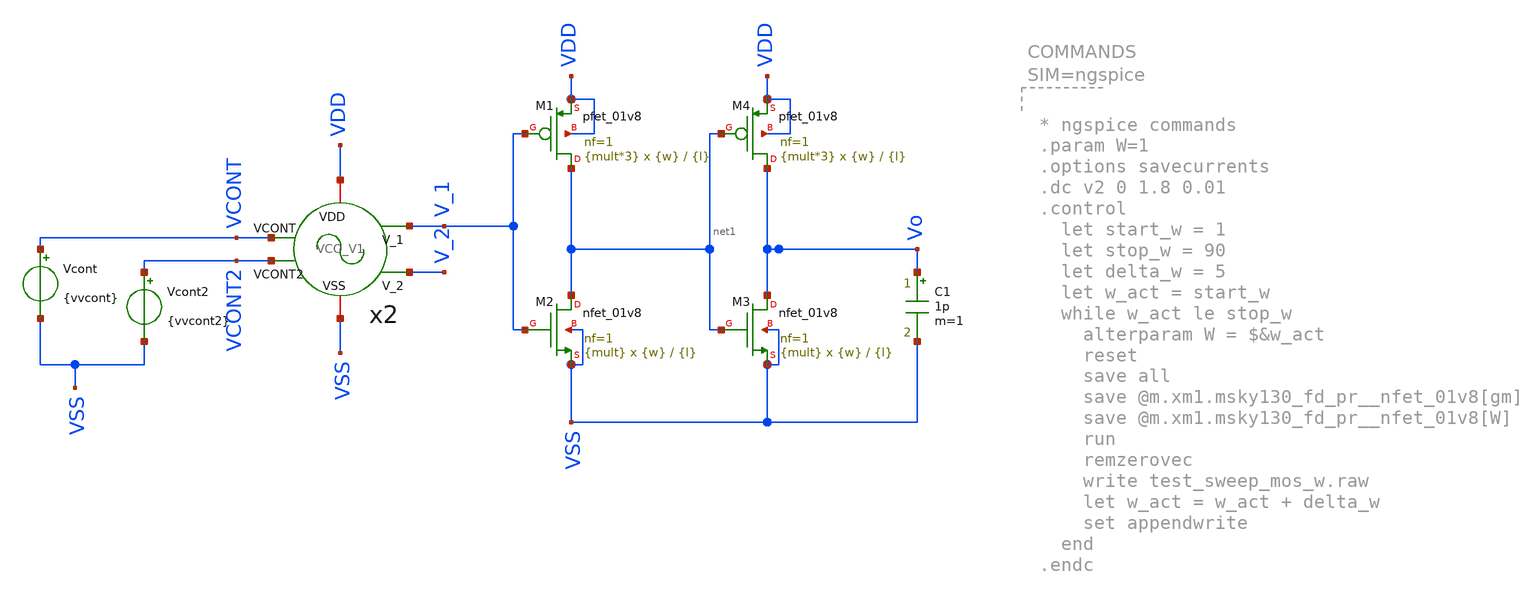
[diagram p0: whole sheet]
** sch_path: xschem/VCO/TB_VCO_VC.sch
**.subckt TB_VCO_VC
XM2 net1 V_1 VSS VSS sky130_fd_pr__nfet_01v8 L={l} W={w} nf=1 ad='int((nf+1)/2) * W/nf * 0.29' as='int((nf+2)/2) * W/nf * 0.29'
+ pd='2*int((nf+1)/2) * (W/nf + 0.29)' ps='2*int((nf+2)/2) * (W/nf + 0.29)' nrd='0.29 / W' nrs='0.29 / W'
+ sa=0 sb=0 sd=0 mult={mult} m={mult}
XM1 net1 V_1 VDD VDD sky130_fd_pr__pfet_01v8 L={l} W={w} nf=1 ad='int((nf+1)/2) * W/nf * 0.29' as='int((nf+2)/2) * W/nf * 0.29'
+ pd='2*int((nf+1)/2) * (W/nf + 0.29)' ps='2*int((nf+2)/2) * (W/nf + 0.29)' nrd='0.29 / W' nrs='0.29 / W'
+ sa=0 sb=0 sd=0 mult={mult*3} m={mult*3}
C1 Vo VSS 1p m=1
XM3 Vo net1 VSS VSS sky130_fd_pr__nfet_01v8 L={l} W={w} nf=1 ad='int((nf+1)/2) * W/nf * 0.29' as='int((nf+2)/2) * W/nf * 0.29'
+ pd='2*int((nf+1)/2) * (W/nf + 0.29)' ps='2*int((nf+2)/2) * (W/nf + 0.29)' nrd='0.29 / W' nrs='0.29 / W'
+ sa=0 sb=0 sd=0 mult={mult} m={mult}
XM4 Vo net1 VDD VDD sky130_fd_pr__pfet_01v8 L={l} W={w} nf=1 ad='int((nf+1)/2) * W/nf * 0.29' as='int((nf+2)/2) * W/nf * 0.29'
+ pd='2*int((nf+1)/2) * (W/nf + 0.29)' ps='2*int((nf+2)/2) * (W/nf + 0.29)' nrd='0.29 / W' nrs='0.29 / W'
+ sa=0 sb=0 sd=0 mult={mult*3} m={mult*3}
Vcont VCONT VSS {vvcont}
Vcont2 VCONT2 VSS {vvcont2}
x2 VCONT VSS VDD V_1 V_2 VCONT2 VCO_V1
**** begin user architecture code

.lib /opt/pdks/sky130A/libs.tech/ngspice/sky130.lib.spice tt
*.lib /opt/pdks/sky130A/libs.tech/ngspice/sky130.lib.spice ss
*.lib /opt/pdks/sky130A/libs.tech/ngspice/sky130.lib.spice ff
*.lib /opt/pdks/sky130A/libs.tech/ngspice/sky130.lib.spice sf
*.lib /opt/pdks/sky130A/libs.tech/ngspice/sky130.lib.spice fs


.param Co = 0.1p
.param mult = 1
.param w = 1
.param l = 0.15

.param vvcont = 0
.param vvcont2 = 0.5

vvdd vdd 0 dc 1.8
vvss vss 0 0
*vvcont VCONT 0 dc 0
*vvcont2 VCONT2 0 dc 0
*.option temp = 200
.ic v(V_1) = 0
.ic v(V_2) = 1.8
.save v(V_1) v(Vo)

.param SimTime =  150u
.csparam SimTime ={Simtime}
.csparam Tmargin = 50u






.tran 5n {SimTime}
.csparam start = 10
.control
let Vtarg = 0.9
compose vin_var start=0.2 stop=0.7 step=0.05

let strt = 0.2
let stp = 0.7
let step = 0.05
let len2 = 1 + (stp-strt)/step
let f_sweep = vector(len2)
let index = 0
foreach val $&vin_var
	alter vcont $val
	let f_sum = 0
	let t_act = 0
	let period_cont = 1
	run
	while t_act le SimTime - Tmargin
		meas tran t_rise WHEN v(Vo) = {Vtarg} RISE = {period_cont}
		let t_act = t_rise
		*print t_act SimTime period_cont
		meas tran T TRIG v(Vo) VAL = {Vtarg} RISE = {period_cont} TARG v(Vo) VAL = {Vtarg}  FALL = {period_cont}
		let f =1/T
		let f_sum = f_sum + f
		let period_cont = period_cont + 1
	end
	*wrdata ../../sim_data/data_VCO_vto1p1.txt tran1.v(V_1) tran2.v(V_1) tran3.v(V_1) tran4.v(V_1)
+ tran5.v(V_1) tran6.v(V_1) tran7.v(V_1) tran8.v(V_1) tran9.v(V_1) tran10.v(V_1) tran11.v(V_1) tran12.v(V_1)
+ tran13.v(V_1) tran14.v(V_1) tran15.v(V_1) tran16.v(V_1) tran17.v(V_1)
	let f_avg = f_sum/(period_cont-1)
	let f_sweep[index] = f_avg
	let index = index +1
end
plot tran1.v(Vo)
plot tran9.v(Vo)
print f_sweep
plot f_sweep vs vin_var
.endc




.param w_MP1a = 0.5
.param l_MP1a = 10
.param w_MP1b = 3.5
.param l_MP1b = 7
.param w_MP2 = 8
.param l_MP2 = 4
.param w_MP3 = 5
.param l_MP3 = 4
.param w_MP4 = 5
.param l_MP4 = 5

.param w_MN1 = 5
.param l_MN1 = 0.5
.param w_MN2 = 5
.param l_MN2 = 0.5
.param w_MN3 = 3
.param l_MN3 = 0.5
.param w_MN4 = 2
.param l_MN4 = 5



**** end user architecture code
**.ends

* expanding   symbol:
*+  /workspaces/usm-vlsi-tools/shared_xserver/simulations/SKY130/IPD500-TimebasedDCDCBuck/VCO/VCO_V1.sym # of pins=6
** sym_path: xschem/VCO/VCO_V1.sym
** sch_path: xschem/VCO/VCO_V1.sch
.subckt VCO_V1 VCONT VSS VDD V_1 V_2 VCONT2
*.ipin VCONT
*.iopin VDD
*.iopin VSS
*.opin V_1
*.opin V_2
*.ipin VCONT2
x1 VDD VCONT V_1 V_5 VSS VCONT2 stage_V1
x2 VDD VCONT V_2 V_1 VSS VCONT2 stage_V1
x3 VDD VCONT V_3 V_2 VSS VCONT2 stage_V1
x4 VDD VCONT V_4 V_3 VSS VCONT2 stage_V1
x5 VDD VCONT V_5 V_4 VSS VCONT2 stage_V1
.ends


* expanding   symbol:  ../VCO/stage_V1.sym # of pins=6
** sym_path: xschem/VCO/stage_V1.sym
** sch_path: xschem/VCO/stage_V1.sch
.subckt stage_V1 VDD VCONT VOUT VIN VSS VCONT2
*.ipin VCONT2
*.ipin VIN
*.opin VOUT
*.iopin VDD
*.iopin VSS
*.ipin VCONT
XMN1 VSS net2 net2 VSS sg13_hv_nmos w={w_MN1} l={l_MN1} ng=1 m={m_MN1} mm_ok=1
XMN2 VSS net2 net3 VSS sg13_hv_nmos w={w_MN2} l={l_MN2} ng=1 m={m_MN2} mm_ok=1
XMN3 VSS net2 VdsMN3 VSS sg13_hv_nmos w={w_MN3} l={l_MN3} ng=1 m={m_MN3} mm_ok=1
XMP1a VCN VCONT VDD VDD sg13_hv_pmos w={w_MP1a} l={l_MP1a} ng=1 m={m_MP1a} mm_ok=1
XMP2 VCP VCP VDD VDD sg13_hv_pmos w={w_MP2} l={l_MP2} ng=1 m={m_MP2} mm_ok=1
XMP3 net4 VCP VDD VDD sg13_hv_pmos w={w_MP3} l={l_MP3} ng=1 m={m_MP3} mm_ok=1
XMP7 net1 VIN VSMP4 VDD sg13_hv_pmos w={w_MP4} l={l_MP4} ng=1 m={m_MP4} mm_ok=1
XMN4 VdsMN3 VIN net1 VSS sg13_hv_nmos w={w_MN4} l={l_MN4} ng=1 m={m_MN4} mm_ok=1
XMP1b VCN VCONT2 VDD VDD sg13_hv_pmos w={w_MP1b} l={l_MP1b} ng=1 m={m_MP1b} mm_ok=1
VIcont1 VCN net2 0
.save i(vicont1)
VIcont2 VCP net3 0
.save i(vicont2)
VIcont3 net4 VSMP4 0
.save i(vicont3)
VIcont4 net1 VOUT 0
.save i(vicont4)
.ends

.end
